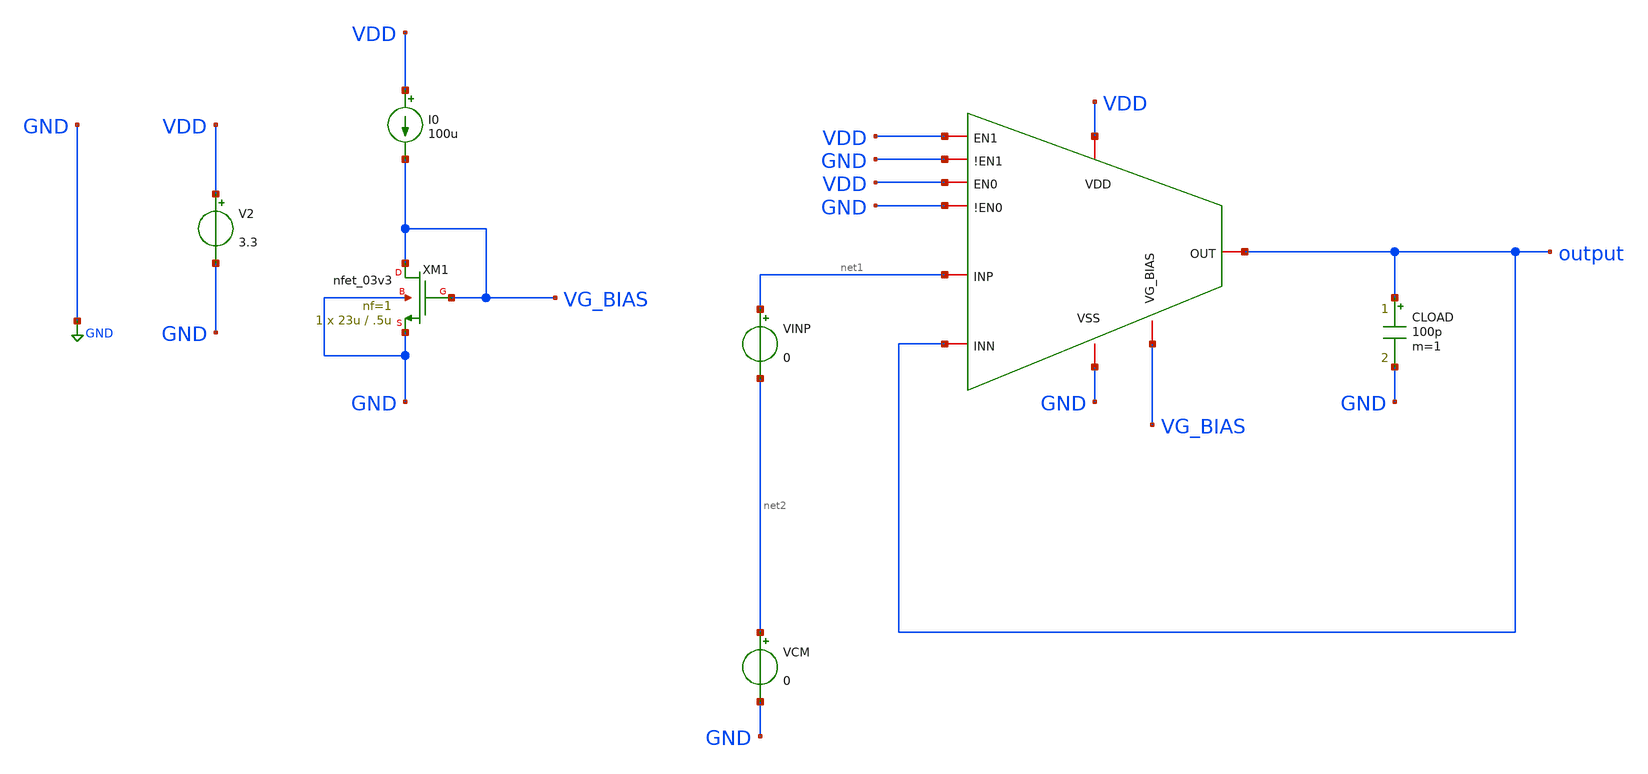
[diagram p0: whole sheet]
** sch_path: designs/libs/core_amps/ota_folded_cascode/programmable_dc_unity_tb.sch
**.subckt programmable_dc_unity_tb
x1 VDD VDD GND GND VDD GND output net1 output VG_BIAS programmable_folded
XM1 VG_BIAS VG_BIAS GND GND nfet_03v3 L=.5u W=23u nf=1 ad='int((nf+1)/2) * W/nf * 0.18u' as='int((nf+2)/2) * W/nf * 0.18u'
+ pd='2*int((nf+1)/2) * (W/nf + 0.18u)' ps='2*int((nf+2)/2) * (W/nf + 0.18u)' nrd='0.18u / W' nrs='0.18u / W'
+ sa=0 sb=0 sd=0 m=1
I0 VDD VG_BIAS 100u
V2 VDD GND 3.3
CLOAD output GND 100p m=1
VINP net1 net2 0
VCM net2 GND 0
**** begin user architecture code

.include $::180MCU_MODELS/design.ngspice
.lib $::180MCU_MODELS/sm141064.ngspice typical



.control

dc VINP 0 4 0.001
let gain = deriv(v(output))
meas dc icmr_low when gain = 0.95 rise = 1
meas dc icmr_high when gain = 0.95 fall = 1
let swing_low = icmr_low
let swing_high = icmr_high
print icmr_low icmr_high
print swing_high - swing_low

plot v(output) gain

.endc


**** end user architecture code
**.ends
.GLOBAL GND
.end
